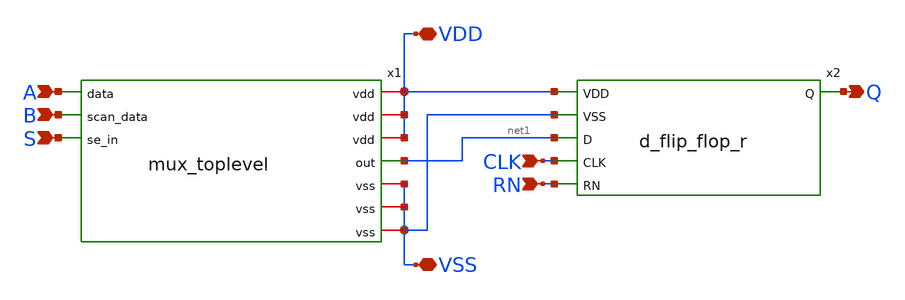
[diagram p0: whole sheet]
** sch_path: designs/libs/sdffrq_tg_toplevel/sdffrq_toplevel.sch
**.subckt sdffrq_toplevel A B S VDD VSS Q RN CLK
*.ipin A
*.ipin B
*.ipin S
*.iopin VDD
*.iopin VSS
*.opin Q
*.ipin RN
*.ipin CLK
x1 VDD A VSS net1 B S mux_toplevel
x2 VDD VSS Q net1 CLK RN d_flip_flop_r
**.ends
.end
